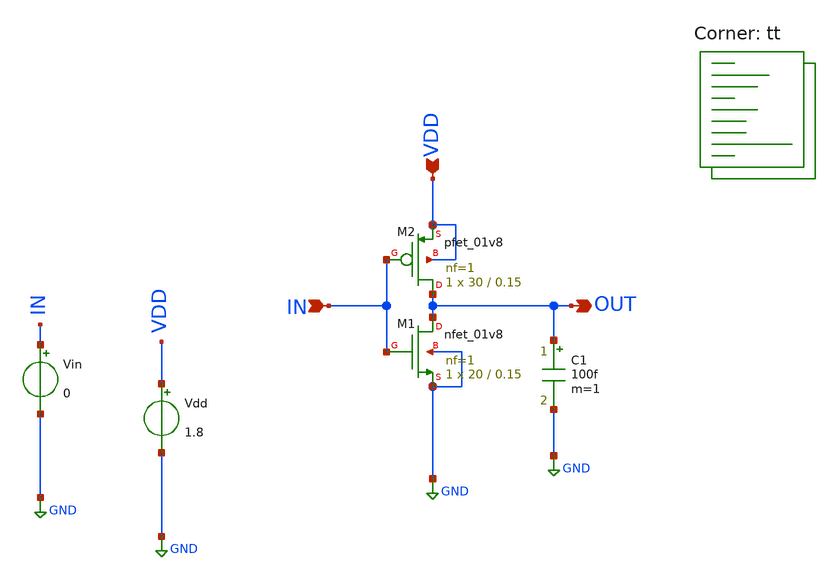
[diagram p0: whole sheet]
** sch_path: sizing-inverter.sch
**.subckt sizing-inverter IN VDD OUT
*.ipin IN
*.ipin VDD
*.opin OUT
Vin IN GND 0
Vdd VDD GND 1.8
XM1 OUT IN GND GND sky130_fd_pr__nfet_01v8 L=0.15 W=20 nf=1 ad='int((nf+1)/2) * W/nf * 0.29' as='int((nf+2)/2) * W/nf * 0.29'
+ pd='2*int((nf+1)/2) * (W/nf + 0.29)' ps='2*int((nf+2)/2) * (W/nf + 0.29)' nrd='0.29 / W' nrs='0.29 / W'
+ sa=0 sb=0 sd=0 mult=1 m=1
XM2 OUT IN VDD VDD sky130_fd_pr__pfet_01v8 L=0.15 W=30 nf=1 ad='int((nf+1)/2) * W/nf * 0.29' as='int((nf+2)/2) * W/nf * 0.29'
+ pd='2*int((nf+1)/2) * (W/nf + 0.29)' ps='2*int((nf+2)/2) * (W/nf + 0.29)' nrd='0.29 / W' nrs='0.29 / W'
+ sa=0 sb=0 sd=0 mult=1 m=1
C1 OUT GND 100f m=1
**** begin user architecture code
.lib $::SKYWATER_MODELS/sky130.lib.spice tt


.options savecurrents


.dc vin 0 1.8 1m


.control
save all


let step=1
let max_w=70
let curr_w=30

let min_diff=100
let best_w=curr_w

let iters = int((max_w - curr_w)/step)
let iter = 0

let switching_points = vector(iters)


while curr_w < max_w

	alter m.xm2.msky130_fd_pr__pfet_01v8 W=curr_w
	run



	meas dc switching_point WHEN v(out)=v(in) CROSS=LAST

	let difference=abs(switching_point - 0.9)
	let switching_points[iter]=switching_point

	set plotswpoint = ( $plotswpoint switching_point )
	set plotstr = ( $plotstr {$curplot}.v(out) )


	if difference < min_diff
		let best_w = curr_w
		let min_diff = difference
	end

	let curr_w=curr_w + step
	let iter=iter + 1


end
set plotstr = ( $plotstr {$curplot}.v(in) )


set nolegend
plot $plotstr
plot switching_points


.endc


**** end user architecture code
**.ends
.GLOBAL GND
.end
